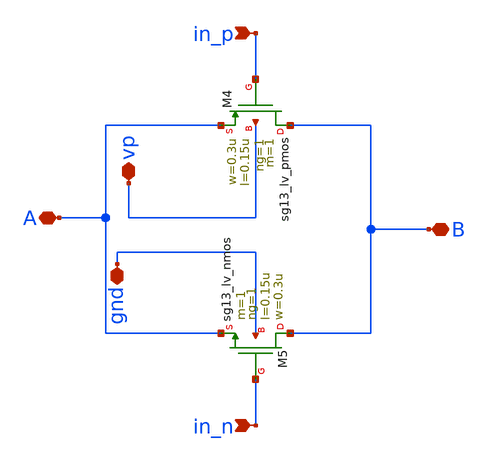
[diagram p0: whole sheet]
** sch_path: PLL0663-main/schematic/xschem/divider/passgate.sch
**.subckt passgate in_n in_p vp gnd B A
*.ipin in_n
*.ipin in_p
*.iopin vp
*.iopin gnd
*.iopin B
*.iopin A
XM4 B in_p A vp sg13_lv_pmos w=0.3u l=0.15u ng=1 m=1 mm_ok=1
XM5 B in_n A gnd sg13_lv_nmos w=0.3u l=0.15u ng=1 m=1 mm_ok=1
**.ends
.end
